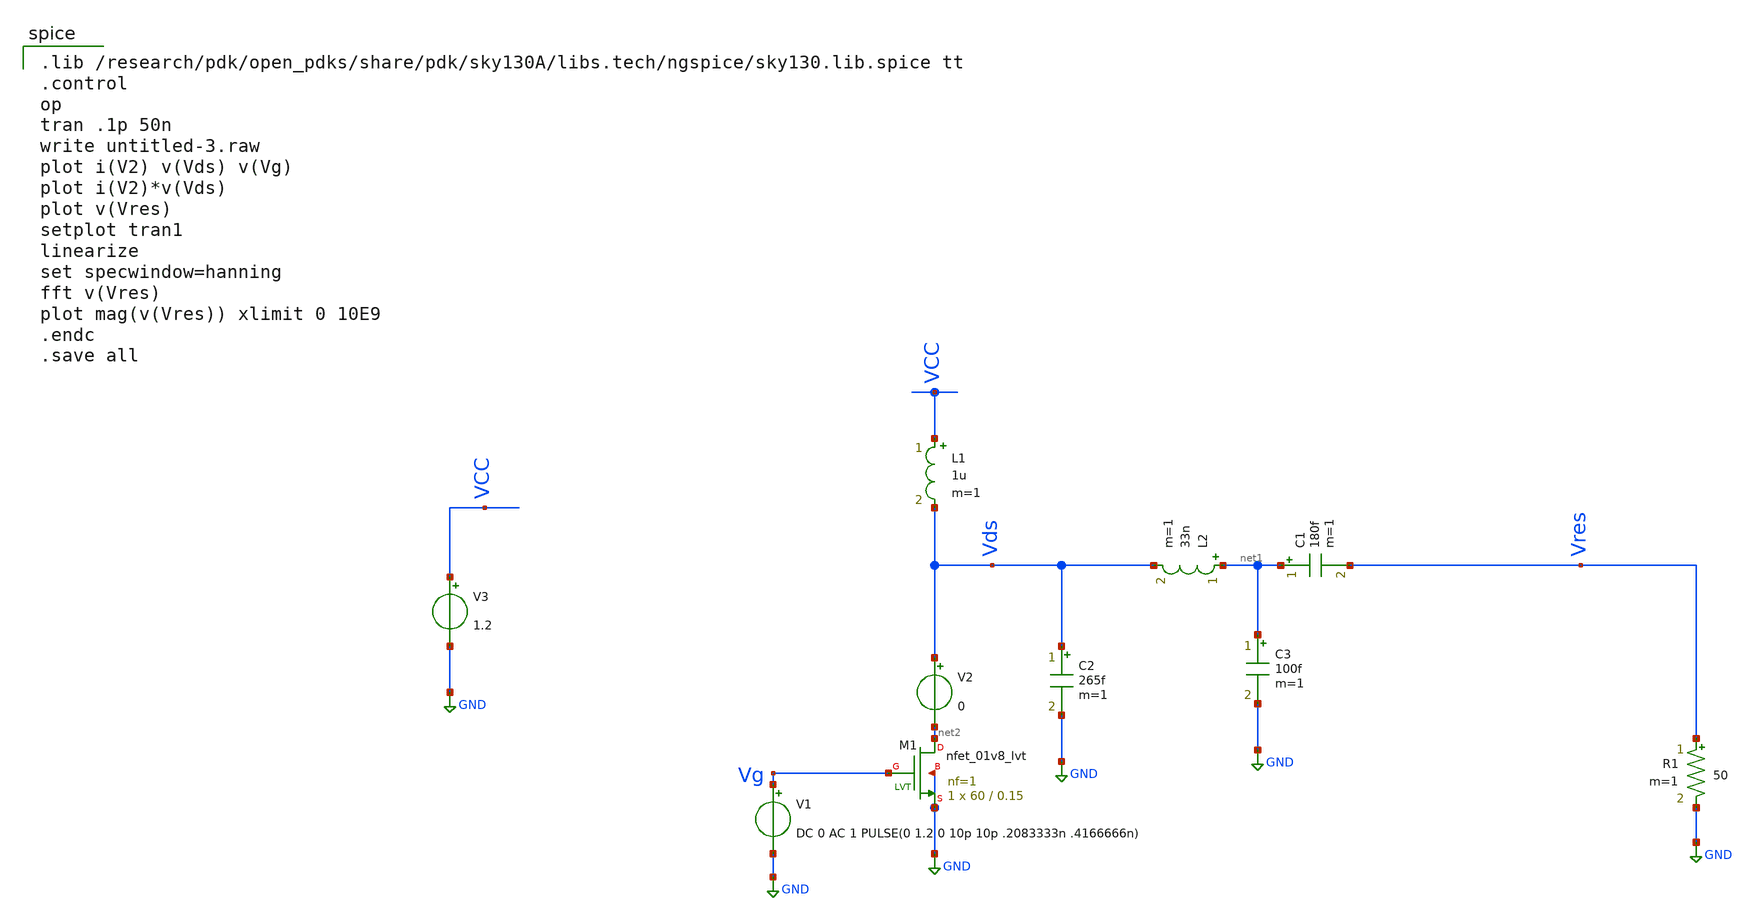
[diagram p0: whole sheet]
** sch_path: skywater_stuff/ECE631_RF_CMOS/power_amp_test.sch
**.subckt power_amp_test
XM1 net2 Vg GND GND sky130_fd_pr__nfet_01v8_lvt L=0.15 W=60 nf=1 ad='int((nf+1)/2) * W/nf * 0.29' as='int((nf+2)/2) * W/nf * 0.29'
+ pd='2*int((nf+1)/2) * (W/nf + 0.29)' ps='2*int((nf+2)/2) * (W/nf + 0.29)' nrd='0.29 / W' nrs='0.29 / W'
+ sa=0 sb=0 sd=0 mult=1 m=1
L1 VCC Vds 1u m=1
L2 net1 Vds 33n m=1
C1 net1 Vres 180f m=1
C2 Vds GND 265f m=1
R1 Vres GND 50 m=1
V2 Vds net2 0
V1 Vg GND DC 0 AC 1 PULSE(0 1.2 0 10p 10p .2083333n .4166666n)
V3 VCC GND 1.2
C3 net1 GND 100f m=1
**** begin user architecture code

.lib /research/pdk/open_pdks/share/pdk/sky130A/libs.tech/ngspice/sky130.lib.spice tt
.control
op
tran .1p 50n
write untitled-3.raw
plot i(V2) v(Vds) v(Vg)
plot i(V2)*v(Vds)
plot v(Vres)
setplot tran1
linearize
set specwindow=hanning
fft v(Vres)
plot mag(v(Vres)) xlimit 0 10E9
.endc
.save all


**** end user architecture code
**.ends
.GLOBAL GND
.end
